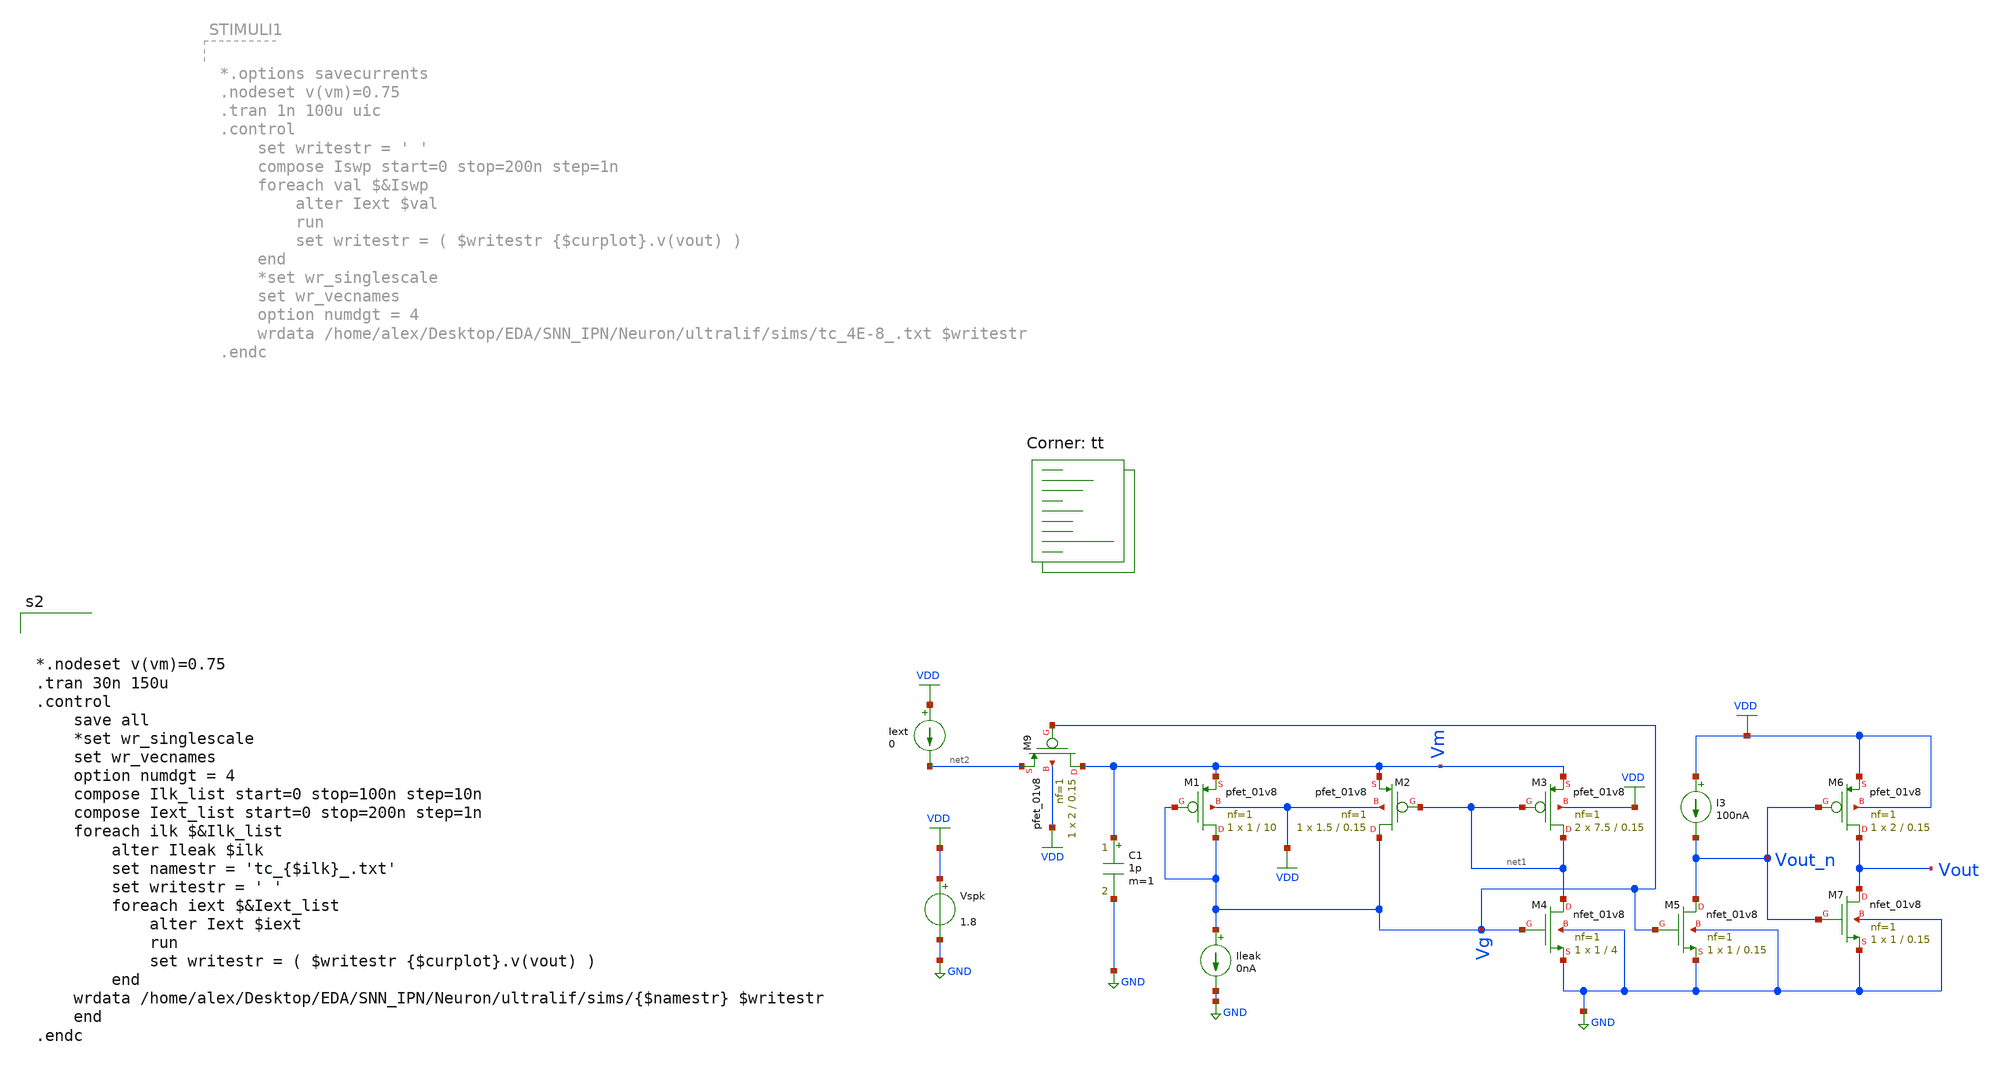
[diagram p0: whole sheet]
** sch_path: Neuron/ultralif/tuning_curve.sch
**.subckt tuning_curve
XM1 Vg Vg Vm VDD sky130_fd_pr__pfet_01v8 L=10 W=1 nf=1 ad='int((nf+1)/2) * W/nf * 0.29' as='int((nf+2)/2) * W/nf * 0.29'
+ pd='2*int((nf+1)/2) * (W/nf + 0.29)' ps='2*int((nf+2)/2) * (W/nf + 0.29)' nrd='0.29 / W' nrs='0.29 / W'
+ sa=0 sb=0 sd=0 mult=1 m=1
XM2 Vg net1 Vm VDD sky130_fd_pr__pfet_01v8 L=0.15 W=1.5 nf=1 ad='int((nf+1)/2) * W/nf * 0.29' as='int((nf+2)/2) * W/nf * 0.29'
+ pd='2*int((nf+1)/2) * (W/nf + 0.29)' ps='2*int((nf+2)/2) * (W/nf + 0.29)' nrd='0.29 / W' nrs='0.29 / W'
+ sa=0 sb=0 sd=0 mult=1 m=1
XM3 net1 net1 Vm VDD sky130_fd_pr__pfet_01v8 L=0.15 W=7.5 nf=1 ad='int((nf+1)/2) * W/nf * 0.29' as='int((nf+2)/2) * W/nf * 0.29'
+ pd='2*int((nf+1)/2) * (W/nf + 0.29)' ps='2*int((nf+2)/2) * (W/nf + 0.29)' nrd='0.29 / W' nrs='0.29 / W'
+ sa=0 sb=0 sd=0 mult=2 m=2
XM4 net1 Vg GND GND sky130_fd_pr__nfet_01v8 L=4 W=1 nf=1 ad='int((1 + 1)/2) * 1 / 1 * 0.29' as='int((1 + 2)/2) * 1 / 1 * 0.29'
+ pd='2*int((1 + 1)/2) * (1 / 1 + 0.29)' ps='2*int((1 + 2)/2) * (1 / 1 + 0.29)' nrd='0.29 / 1 ' nrs='0.29 / 1 '
+ sa=0 sb=0 sd=0 mult=1 m=1
XM5 Vout_n Vg GND GND sky130_fd_pr__nfet_01v8 L=0.15 W=1 nf=1 ad='int((1 + 1)/2) * 1 / 1 * 0.29' as='int((1 + 2)/2) * 1 / 1 * 0.29'
+ pd='2*int((1 + 1)/2) * (1 / 1 + 0.29)' ps='2*int((1 + 2)/2) * (1 / 1 + 0.29)' nrd='0.29 / 1 ' nrs='0.29 / 1 '
+ sa=0 sb=0 sd=0 mult=1 m=1
XM6 Vout Vout_n VDD VDD sky130_fd_pr__pfet_01v8 L=0.15 W=2 nf=1 ad='int((nf+1)/2) * W/nf * 0.29' as='int((nf+2)/2) * W/nf * 0.29'
+ pd='2*int((nf+1)/2) * (W/nf + 0.29)' ps='2*int((nf+2)/2) * (W/nf + 0.29)' nrd='0.29 / W' nrs='0.29 / W'
+ sa=0 sb=0 sd=0 mult=1 m=1
XM7 Vout Vout_n GND GND sky130_fd_pr__nfet_01v8 L=0.15 W=1 nf=1 ad='int((1 + 1)/2) * 1 / 1 * 0.29' as='int((1 + 2)/2) * 1 / 1 * 0.29'
+ pd='2*int((1 + 1)/2) * (1 / 1 + 0.29)' ps='2*int((1 + 2)/2) * (1 / 1 + 0.29)' nrd='0.29 / 1 ' nrs='0.29 / 1 '
+ sa=0 sb=0 sd=0 mult=1 m=1
Ileak Vg GND 0nA
Vspk VDD GND 1.8
C1 Vm GND 1p m=1
Iext VDD net2 0
I3 VDD Vout_n 100nA
XM9 Vm Vg net2 VDD sky130_fd_pr__pfet_01v8 L=0.15 W=2 nf=1 ad='int((nf+1)/2) * W/nf * 0.29' as='int((nf+2)/2) * W/nf * 0.29'
+ pd='2*int((nf+1)/2) * (W/nf + 0.29)' ps='2*int((nf+2)/2) * (W/nf + 0.29)' nrd='0.29 / W' nrs='0.29 / W'
+ sa=0 sb=0 sd=0 mult=1 m=1
**** begin user architecture code
.lib $::SKYWATER_MODELS/sky130.lib.spice tt



*.nodeset v(vm)=0.75
.tran 30n 150u
.control
	save all
	*set wr_singlescale
	set wr_vecnames
	option numdgt = 4
	compose Ilk_list start=0 stop=100n step=10n
	compose Iext_list start=0 stop=200n step=1n
    foreach ilk $&Ilk_list
        alter Ileak $ilk
        set namestr = 'tc_{$ilk}_.txt'
        set writestr = ' '
        foreach iext $&Iext_list
            alter Iext $iext
            run
            set writestr = ( $writestr {$curplot}.v(vout) )
        end
	wrdata /home/alex/Desktop/EDA/SNN_IPN/Neuron/ultralif/sims/{$namestr} $writestr
    end
.endc


**** end user architecture code
**.ends
.GLOBAL GND
.GLOBAL VDD
.end
